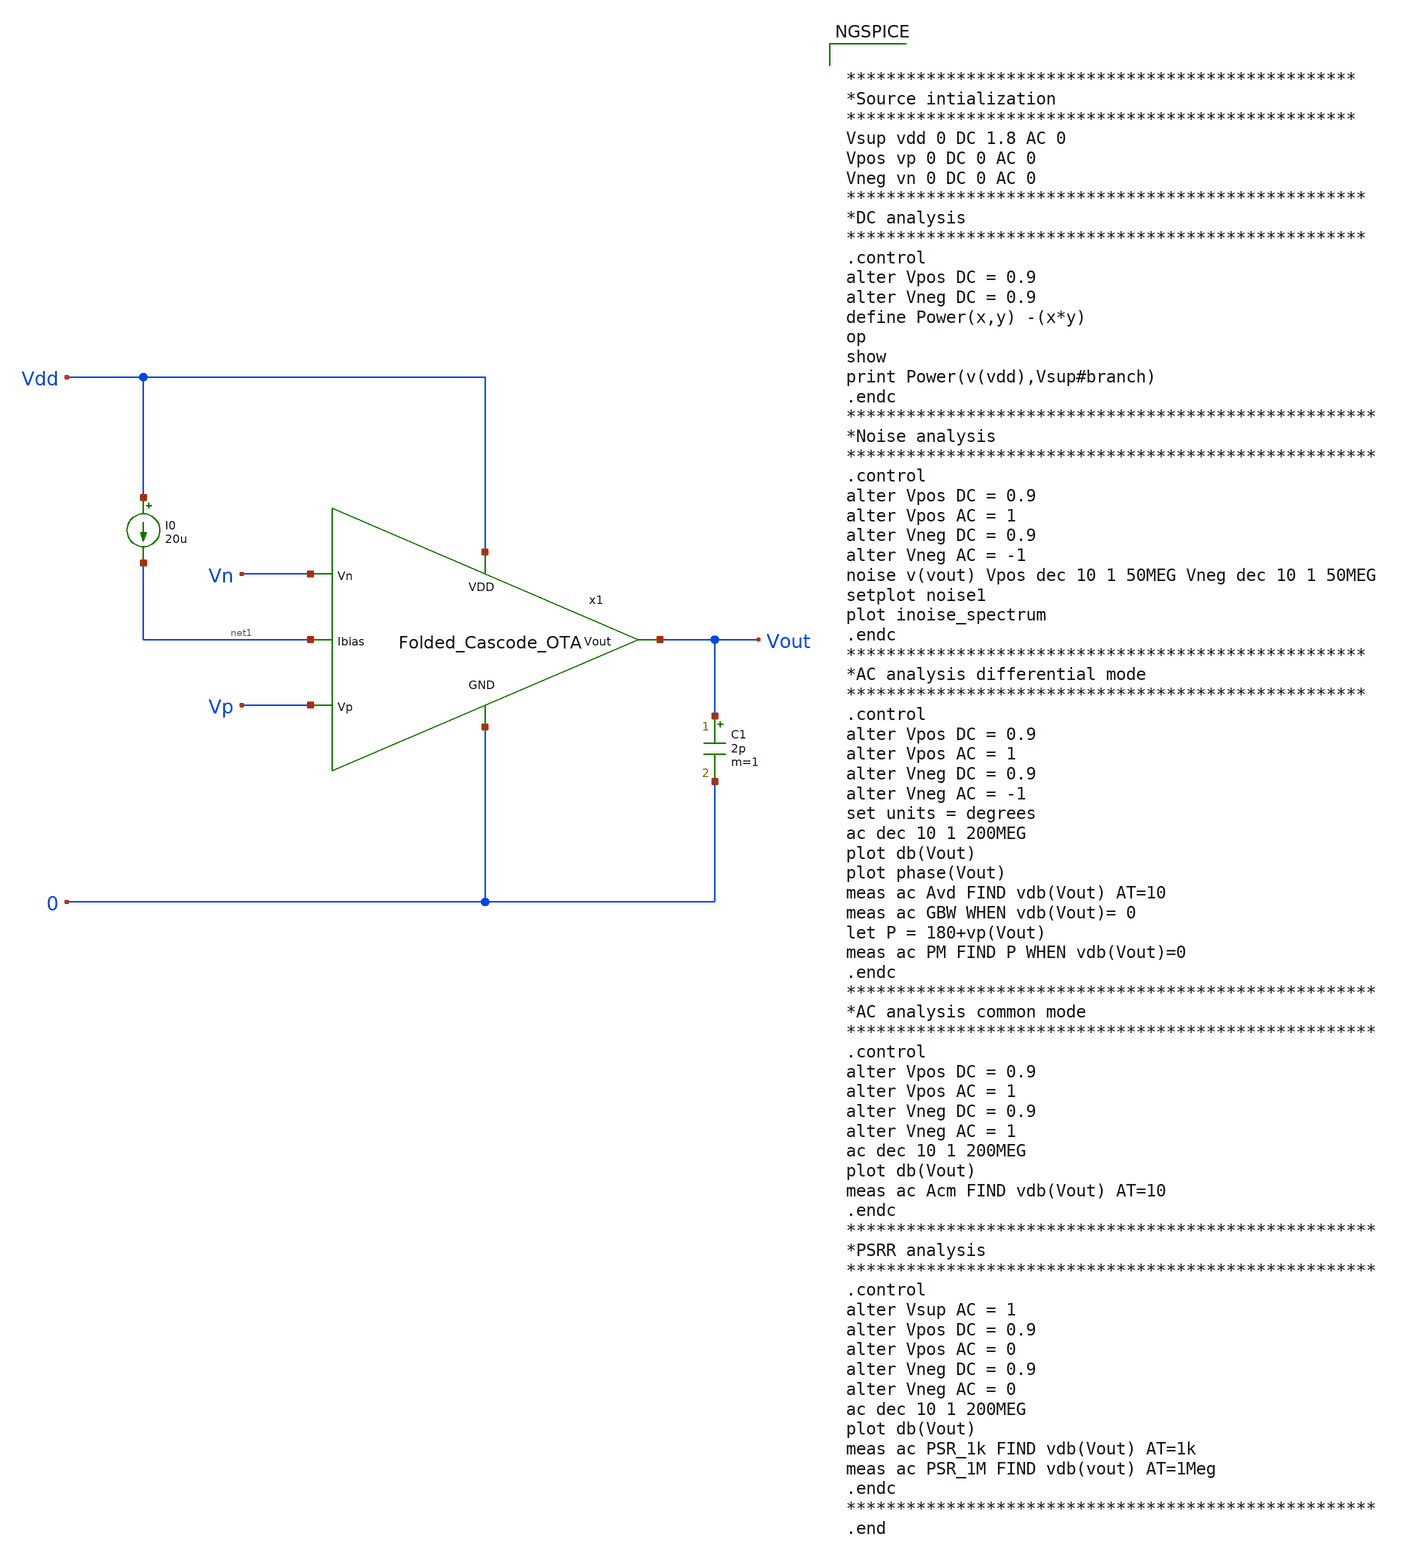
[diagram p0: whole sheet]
** sch_path: Analog_Blocks/OTA/Testbench/Folded_Cascode/Transistor1.8v/Folded_Cascode1.8v_meas.sch
**.subckt Folded_Cascode1.8v_meas
I0 Vdd net1 20u
C1 Vout 0 2p m=1
x1 Vdd Vout Vp Vn net1 0 Folded_Cascode_OTA
**** begin user architecture code

.include ~/Analog_blocks/models/skywater-pdk/libraries/sky130_fd_pr/latest/cells/nfet_01v8/sky130_fd_pr__nfet_01v8__tt.corner.spice
.include ~/Analog_blocks/models/skywater-pdk/libraries/sky130_fd_pr/latest/cells/nfet_01v8_lvt/sky130_fd_pr__nfet_01v8_lvt__tt.corner.spice
.include ~/Analog_blocks/models/skywater-pdk/libraries/sky130_fd_pr/latest/cells/pfet_01v8/sky130_fd_pr__pfet_01v8__tt.corner.spice
.include ~/Analog_blocks/models/skywater-pdk/libraries/sky130_fd_pr/latest/cells/nfet_03v3_nvt/sky130_fd_pr__nfet_03v3_nvt__tt.corner.spice
.include ~/Analog_blocks/models/skywater-pdk/libraries/sky130_fd_pr/latest/cells/nfet_05v0_nvt/sky130_fd_pr__nfet_05v0_nvt__tt.corner.spice
.include ~/Analog_blocks/models/skywater-pdk/libraries/sky130_fd_pr/latest/cells/esd_nfet_01v8/sky130_fd_pr__esd_nfet_01v8__tt.corner.spice
.include ~/Analog_blocks/models/skywater-pdk/libraries/sky130_fd_pr/latest/cells/pfet_01v8_lvt/sky130_fd_pr__pfet_01v8_lvt__tt.corner.spice
.include ~/Analog_blocks/models/skywater-pdk/libraries/sky130_fd_pr/latest/cells/pfet_01v8_hvt/sky130_fd_pr__pfet_01v8_hvt__tt.corner.spice
.include ~/Analog_blocks/models/skywater-pdk/libraries/sky130_fd_pr/latest/cells/esd_pfet_g5v0d10v5/sky130_fd_pr__esd_pfet_g5v0d10v5__tt.corner.spice
.include ~/Analog_blocks/models/skywater-pdk/libraries/sky130_fd_pr/latest/cells/pfet_g5v0d10v5/sky130_fd_pr__pfet_g5v0d10v5__tt.corner.spice
.include ~/Analog_blocks/models/skywater-pdk/libraries/sky130_fd_pr/latest/cells/pfet_g5v0d16v0/sky130_fd_pr__pfet_g5v0d16v0__tt.corner.spice
.include ~/Analog_blocks/models/skywater-pdk/libraries/sky130_fd_pr/latest/cells/nfet_g5v0d10v5/sky130_fd_pr__nfet_g5v0d10v5__tt.corner.spice
.include ~/Analog_blocks/models/skywater-pdk/libraries/sky130_fd_pr/latest/cells/nfet_g5v0d16v0/sky130_fd_pr__nfet_g5v0d16v0__tt_discrete.corner.spice
.include ~/Analog_blocks/models/skywater-pdk/libraries/sky130_fd_pr/latest/cells/esd_nfet_g5v0d10v5/sky130_fd_pr__esd_nfet_g5v0d10v5__tt.corner.spice
.include ~/Analog_blocks/models/skywater-pdk/libraries/sky130_fd_pr/latest/models/corners/tt/nonfet.spice
* Mismatch parameters
.include ~/Analog_blocks/models/skywater-pdk/libraries/sky130_fd_pr/latest/cells/nfet_01v8/sky130_fd_pr__nfet_01v8__mismatch.corner.spice
.include ~/Analog_blocks/models/skywater-pdk/libraries/sky130_fd_pr/latest/cells/pfet_01v8/sky130_fd_pr__pfet_01v8__mismatch.corner.spice
.include ~/Analog_blocks/models/skywater-pdk/libraries/sky130_fd_pr/latest/cells/nfet_01v8_lvt/sky130_fd_pr__nfet_01v8_lvt__mismatch.corner.spice
.include ~/Analog_blocks/models/skywater-pdk/libraries/sky130_fd_pr/latest/cells/pfet_01v8_lvt/sky130_fd_pr__pfet_01v8_lvt__mismatch.corner.spice
.include ~/Analog_blocks/models/skywater-pdk/libraries/sky130_fd_pr/latest/cells/pfet_01v8_hvt/sky130_fd_pr__pfet_01v8_hvt__mismatch.corner.spice
.include ~/Analog_blocks/models/skywater-pdk/libraries/sky130_fd_pr/latest/cells/nfet_g5v0d10v5/sky130_fd_pr__nfet_g5v0d10v5__mismatch.corner.spice
.include ~/Analog_blocks/models/skywater-pdk/libraries/sky130_fd_pr/latest/cells/pfet_g5v0d10v5/sky130_fd_pr__pfet_g5v0d10v5__mismatch.corner.spice
.include ~/Analog_blocks/models/skywater-pdk/libraries/sky130_fd_pr/latest/cells/nfet_05v0_nvt/sky130_fd_pr__nfet_05v0_nvt__mismatch.corner.spice
.include ~/Analog_blocks/models/skywater-pdk/libraries/sky130_fd_pr/latest/cells/nfet_03v3_nvt/sky130_fd_pr__nfet_03v3_nvt__mismatch.corner.spice
* Resistor
.include ~/Analog_blocks/models/skywater-pdk/libraries/sky130_fd_pr/latest/models/r+c/res_typical__cap_typical.spice
.include ~/Analog_blocks/models/skywater-pdk/libraries/sky130_fd_pr/latest/models/r+c/res_typical__cap_typical__lin.spice
* Special cells
.include ~/Analog_blocks/models/skywater-pdk/libraries/sky130_fd_pr/latest/models/corners/tt/specialized_cells.spice
* All models
.include ~/Analog_blocks/models/skywater-pdk/libraries/sky130_fd_pr/latest/models/all.spice
* Corner
.include ~/Analog_blocks/models/skywater-pdk/libraries/sky130_fd_pr/latest/models/corners/tt/rf.spice



***************************************************
*Source intialization
***************************************************
Vsup vdd 0 DC 1.8 AC 0
Vpos vp 0 DC 0 AC 0
Vneg vn 0 DC 0 AC 0
****************************************************
*DC analysis
****************************************************
.control
alter Vpos DC = 0.9
alter Vneg DC = 0.9
define Power(x,y) -(x*y)
op
show
print Power(v(vdd),Vsup#branch)
.endc
*****************************************************
*Noise analysis
*****************************************************
.control
alter Vpos DC = 0.9
alter Vpos AC = 1
alter Vneg DC = 0.9
alter Vneg AC = -1
noise v(vout) Vpos dec 10 1 50MEG Vneg dec 10 1 50MEG
setplot noise1
plot inoise_spectrum
.endc
****************************************************
*AC analysis differential mode
****************************************************
.control
alter Vpos DC = 0.9
alter Vpos AC = 1
alter Vneg DC = 0.9
alter Vneg AC = -1
set units = degrees
ac dec 10 1 200MEG
plot db(Vout)
plot phase(Vout)
meas ac Avd FIND vdb(Vout) AT=10
meas ac GBW WHEN vdb(Vout)= 0
let P = 180+vp(Vout)
meas ac PM FIND P WHEN vdb(Vout)=0
.endc
*****************************************************
*AC analysis common mode
*****************************************************
.control
alter Vpos DC = 0.9
alter Vpos AC = 1
alter Vneg DC = 0.9
alter Vneg AC = 1
ac dec 10 1 200MEG
plot db(Vout)
meas ac Acm FIND vdb(Vout) AT=10
.endc
*****************************************************
*PSRR analysis
*****************************************************
.control
alter Vsup AC = 1
alter Vpos DC = 0.9
alter Vpos AC = 0
alter Vneg DC = 0.9
alter Vneg AC = 0
ac dec 10 1 200MEG
plot db(Vout)
meas ac PSR_1k FIND vdb(Vout) AT=1k
meas ac PSR_1M FIND vdb(vout) AT=1Meg
.endc
*****************************************************
.end


**** end user architecture code
**.ends
.end
